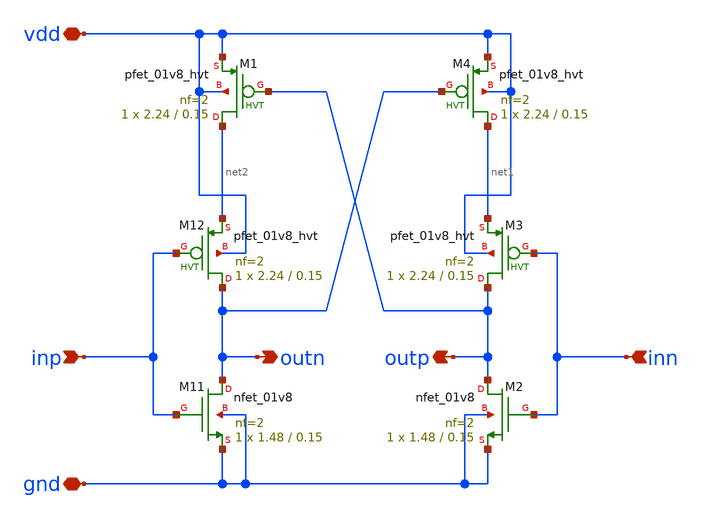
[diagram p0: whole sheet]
** sch_path: xschem/ejf_pll96_vco_ls.sch
**.subckt ejf_pll96_vco_ls inp outn inn outp vdd gnd
*.ipin inp
*.opin outn
*.ipin inn
*.opin outp
*.iopin vdd
*.iopin gnd
XM11 outn inp gnd gnd sky130_fd_pr__nfet_01v8 L=0.15 W=1.48 nf=2 ad='int((nf+1)/2) * W/nf * 0.29' as='int((nf+2)/2) * W/nf * 0.29'
+ pd='2*int((nf+1)/2) * (W/nf + 0.29)' ps='2*int((nf+2)/2) * (W/nf + 0.29)' nrd='0.29 / W' nrs='0.29 / W'
+ sa=0 sb=0 sd=0 mult=1 m=1
XM12 outn inp net2 vdd sky130_fd_pr__pfet_01v8_hvt L=0.15 W=2.24 nf=2 ad='int((nf+1)/2) * W/nf * 0.29'
+ as='int((nf+2)/2) * W/nf * 0.29' pd='2*int((nf+1)/2) * (W/nf + 0.29)' ps='2*int((nf+2)/2) * (W/nf + 0.29)'
+ nrd='0.29 / W' nrs='0.29 / W' sa=0 sb=0 sd=0 mult=1 m=1
XM1 net2 outp vdd vdd sky130_fd_pr__pfet_01v8_hvt L=0.15 W=2.24 nf=2 ad='int((nf+1)/2) * W/nf * 0.29'
+ as='int((nf+2)/2) * W/nf * 0.29' pd='2*int((nf+1)/2) * (W/nf + 0.29)' ps='2*int((nf+2)/2) * (W/nf + 0.29)'
+ nrd='0.29 / W' nrs='0.29 / W' sa=0 sb=0 sd=0 mult=1 m=1
XM2 outp inn gnd gnd sky130_fd_pr__nfet_01v8 L=0.15 W=1.48 nf=2 ad='int((nf+1)/2) * W/nf * 0.29' as='int((nf+2)/2) * W/nf * 0.29'
+ pd='2*int((nf+1)/2) * (W/nf + 0.29)' ps='2*int((nf+2)/2) * (W/nf + 0.29)' nrd='0.29 / W' nrs='0.29 / W'
+ sa=0 sb=0 sd=0 mult=1 m=1
XM3 outp inn net1 vdd sky130_fd_pr__pfet_01v8_hvt L=0.15 W=2.24 nf=2 ad='int((nf+1)/2) * W/nf * 0.29'
+ as='int((nf+2)/2) * W/nf * 0.29' pd='2*int((nf+1)/2) * (W/nf + 0.29)' ps='2*int((nf+2)/2) * (W/nf + 0.29)'
+ nrd='0.29 / W' nrs='0.29 / W' sa=0 sb=0 sd=0 mult=1 m=1
XM4 net1 outn vdd vdd sky130_fd_pr__pfet_01v8_hvt L=0.15 W=2.24 nf=2 ad='int((nf+1)/2) * W/nf * 0.29'
+ as='int((nf+2)/2) * W/nf * 0.29' pd='2*int((nf+1)/2) * (W/nf + 0.29)' ps='2*int((nf+2)/2) * (W/nf + 0.29)'
+ nrd='0.29 / W' nrs='0.29 / W' sa=0 sb=0 sd=0 mult=1 m=1
**.ends
.end
